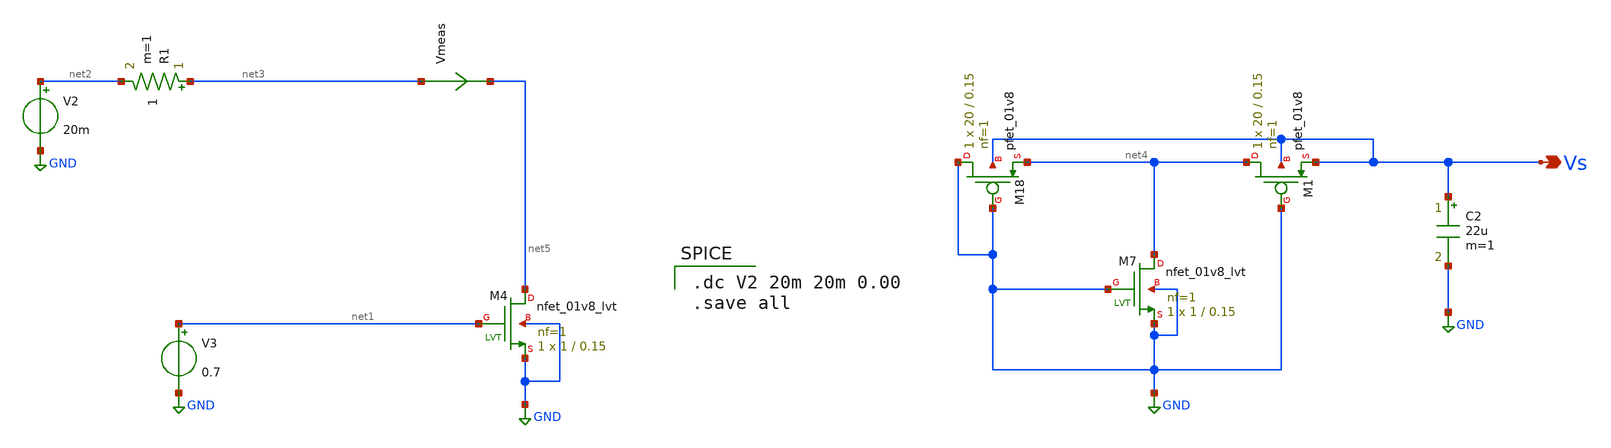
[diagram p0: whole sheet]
** sch_path: Blocks/Startup Converter/Dynamic_res_nmos_lvt.sch
**.subckt Dynamic_res_nmos_lvt Vs
*.opin Vs
C2 Vs GND 22u m=1
XM4 net5 net1 GND GND sky130_fd_pr__nfet_01v8_lvt L=0.15 W=1 nf=1 ad='int((nf+1)/2) * W/nf * 0.29' as='int((nf+2)/2) * W/nf * 0.29'
+ pd='2*int((nf+1)/2) * (W/nf + 0.29)' ps='2*int((nf+2)/2) * (W/nf + 0.29)' nrd='0.29 / W' nrs='0.29 / W'
+ sa=0 sb=0 sd=0 mult=1 m=1
XM7 net4 GND GND GND sky130_fd_pr__nfet_01v8_lvt L=0.15 W=1 nf=1 ad='int((nf+1)/2) * W/nf * 0.29' as='int((nf+2)/2) * W/nf * 0.29'
+ pd='2*int((nf+1)/2) * (W/nf + 0.29)' ps='2*int((nf+2)/2) * (W/nf + 0.29)' nrd='0.29 / W' nrs='0.29 / W'
+ sa=0 sb=0 sd=0 mult=1 m=1
V2 net2 GND 20m
XM18 GND GND net4 Vs sky130_fd_pr__pfet_01v8 L=0.15 W=20 nf=1 ad='int((nf+1)/2) * W/nf * 0.29' as='int((nf+2)/2) * W/nf * 0.29'
+ pd='2*int((nf+1)/2) * (W/nf + 0.29)' ps='2*int((nf+2)/2) * (W/nf + 0.29)' nrd='0.29 / W' nrs='0.29 / W'
+ sa=0 sb=0 sd=0 mult=1 m=1
XM1 net4 GND Vs Vs sky130_fd_pr__pfet_01v8 L=0.15 W=20 nf=1 ad='int((nf+1)/2) * W/nf * 0.29' as='int((nf+2)/2) * W/nf * 0.29'
+ pd='2*int((nf+1)/2) * (W/nf + 0.29)' ps='2*int((nf+2)/2) * (W/nf + 0.29)' nrd='0.29 / W' nrs='0.29 / W'
+ sa=0 sb=0 sd=0 mult=1 m=1
V3 net1 GND 0.7
R1 net3 net2 1 m=1
Vmeas net3 net5 0
.save i(vmeas)
**** begin user architecture code

** opencircuitdesign pdks install
.lib $::SKYWATER_MODELS/sky130.lib.spice tt



.dc V2 20m 20m 0.00
.save all

**** end user architecture code
**.ends
.GLOBAL GND
.end
